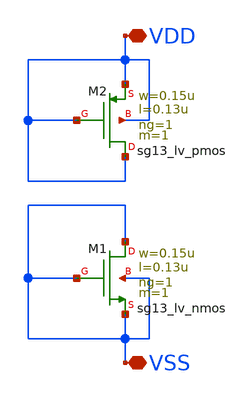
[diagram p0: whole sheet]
** sch_path: ADC8711-main/schematic/xschem/fillers.sch
**.subckt fillers VDD VSS
*.iopin VDD
*.iopin VSS
XM2 VDD VDD VDD VDD sg13_lv_pmos w=0.15u l=0.13u ng=1 m=1 mm_ok=1
XM1 VSS VSS VSS VSS sg13_lv_nmos w=0.15u l=0.13u ng=1 m=1 mm_ok=1
**.ends
.end
